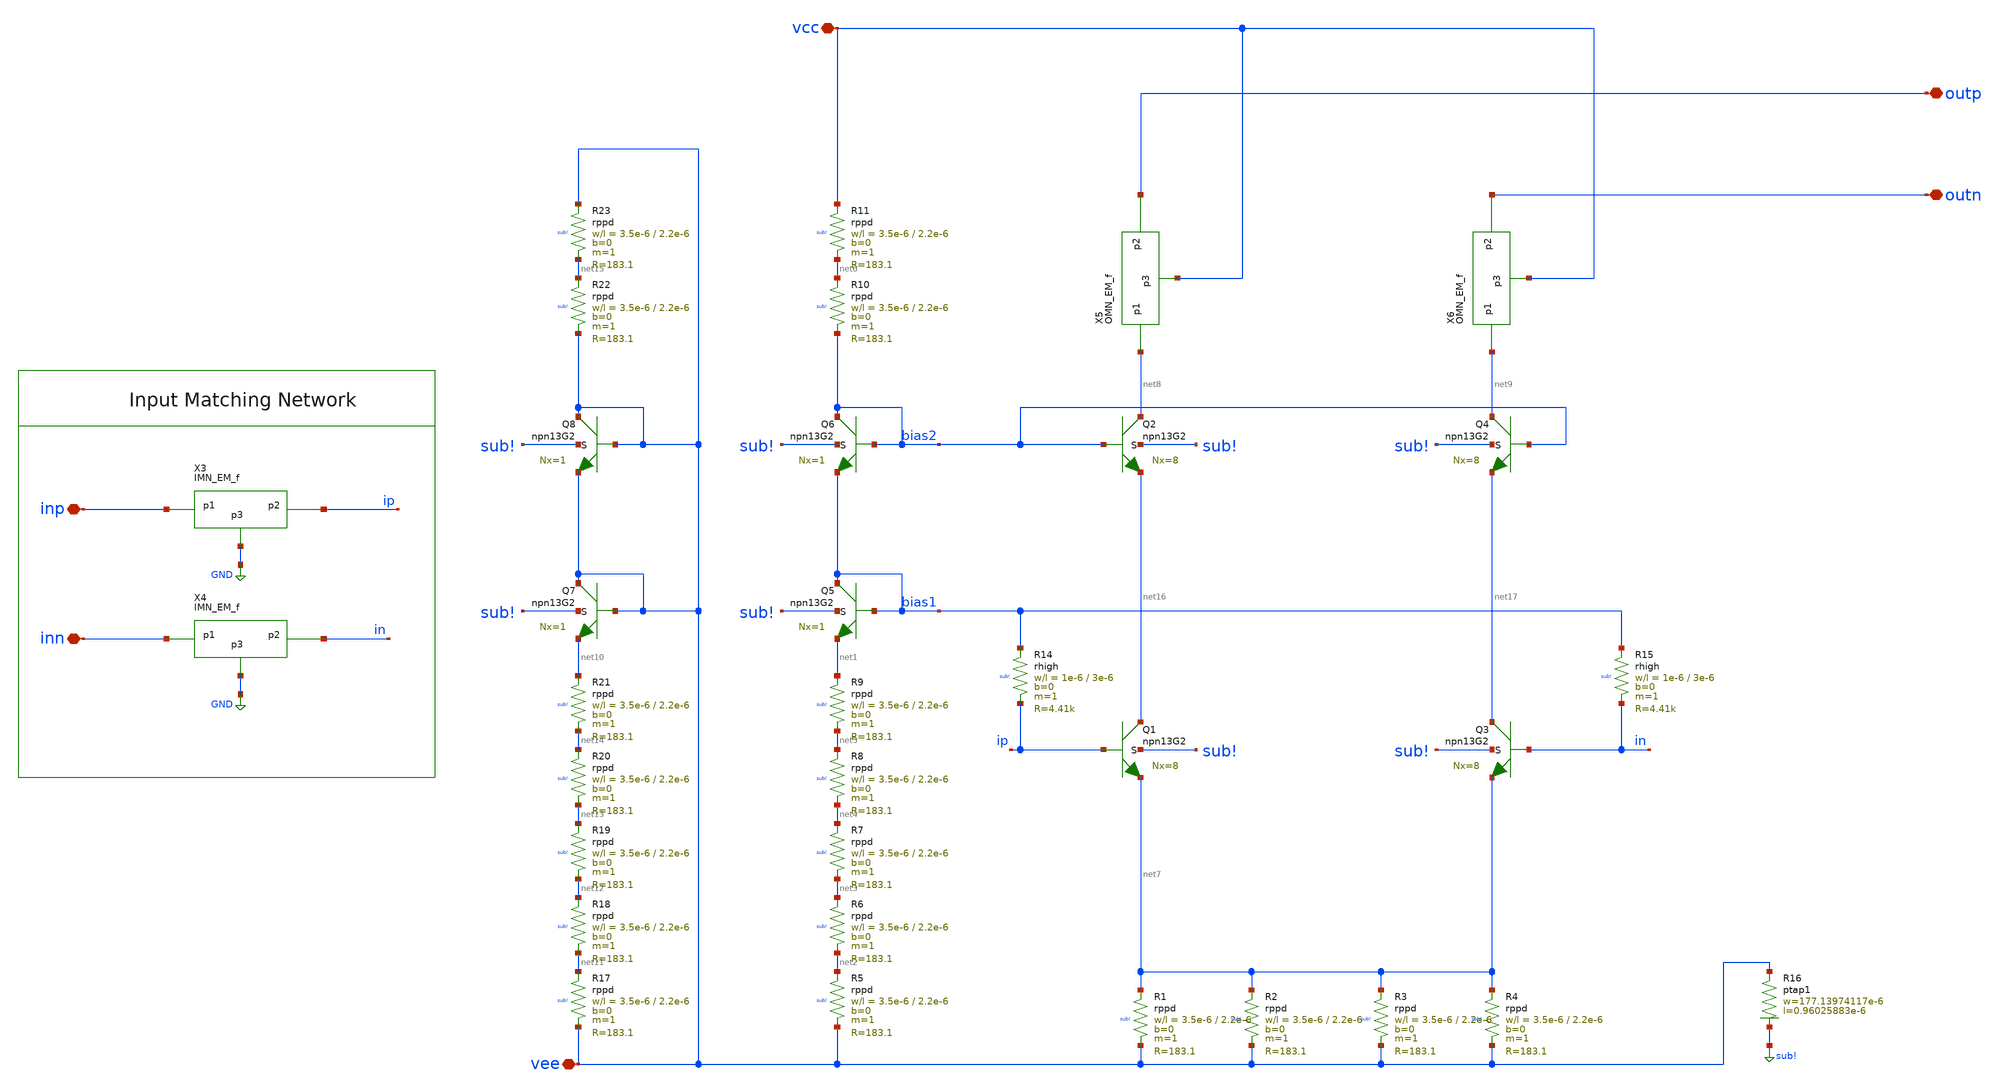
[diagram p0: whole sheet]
** sch_path: LNA0379-main/schematic/xschem/LNA0379_coreEM.sch
**.subckt LNA0379_coreEM inp inn vcc vee outp outn
*.iopin inp
*.iopin inn
*.iopin vcc
*.iopin vee
*.iopin outp
*.iopin outn
XQ1 net16 ip net7 sub! npn13G2 Nx=8 mm_ok=1
XQ2 net8 bias2 net16 sub! npn13G2 Nx=8 mm_ok=1
XQ3 net17 in net7 sub! npn13G2 Nx=8 mm_ok=1
XQ4 net9 bias2 net17 sub! npn13G2 Nx=8 mm_ok=1
XQ5 bias1 bias1 net1 sub! npn13G2 Nx=1 mm_ok=1
XQ6 bias2 bias2 bias1 sub! npn13G2 Nx=1 mm_ok=1
XR14 bias1 ip sub! rhigh w=1e-6 l=3e-6 m=1 b=0 mm_ok=1
XR15 bias1 in sub! rhigh w=1e-6 l=3e-6 m=1 b=0 mm_ok=1
XR1 net7 vee sub! rppd w=3.5e-6 l=2.2e-6 m=1 b=0 mm_ok=1
XR16 vee sub! ptap1 R=1.862 w=177.13974117e-6 l=0.96025883e-6
XX5 net8 outp vcc OMN_EM_f
XX3 inp ip GND IMN_EM_f
XX4 inn in GND IMN_EM_f
XX6 net9 outn vcc OMN_EM_f
XQ7 vee vee net10 sub! npn13G2 Nx=1 mm_ok=1
XQ8 vee vee vee sub! npn13G2 Nx=1 mm_ok=1
XR2 net7 vee sub! rppd w=3.5e-6 l=2.2e-6 m=1 b=0 mm_ok=1
XR3 net7 vee sub! rppd w=3.5e-6 l=2.2e-6 m=1 b=0 mm_ok=1
XR4 net7 vee sub! rppd w=3.5e-6 l=2.2e-6 m=1 b=0 mm_ok=1
XR5 net2 vee sub! rppd w=3.5e-6 l=2.2e-6 m=1 b=0 mm_ok=1
XR6 net3 net2 sub! rppd w=3.5e-6 l=2.2e-6 m=1 b=0 mm_ok=1
XR7 net4 net3 sub! rppd w=3.5e-6 l=2.2e-6 m=1 b=0 mm_ok=1
XR8 net5 net4 sub! rppd w=3.5e-6 l=2.2e-6 m=1 b=0 mm_ok=1
XR9 net1 net5 sub! rppd w=3.5e-6 l=2.2e-6 m=1 b=0 mm_ok=1
XR10 net6 bias2 sub! rppd w=3.5e-6 l=2.2e-6 m=1 b=0 mm_ok=1
XR11 vcc net6 sub! rppd w=3.5e-6 l=2.2e-6 m=1 b=0 mm_ok=1
XR17 net11 vee sub! rppd w=3.5e-6 l=2.2e-6 m=1 b=0 mm_ok=1
XR18 net12 net11 sub! rppd w=3.5e-6 l=2.2e-6 m=1 b=0 mm_ok=1
XR19 net13 net12 sub! rppd w=3.5e-6 l=2.2e-6 m=1 b=0 mm_ok=1
XR20 net14 net13 sub! rppd w=3.5e-6 l=2.2e-6 m=1 b=0 mm_ok=1
XR21 net10 net14 sub! rppd w=3.5e-6 l=2.2e-6 m=1 b=0 mm_ok=1
XR22 net15 vee sub! rppd w=3.5e-6 l=2.2e-6 m=1 b=0 mm_ok=1
XR23 vee net15 sub! rppd w=3.5e-6 l=2.2e-6 m=1 b=0 mm_ok=1
**.ends
.GLOBAL sub!
.GLOBAL GND
.end
